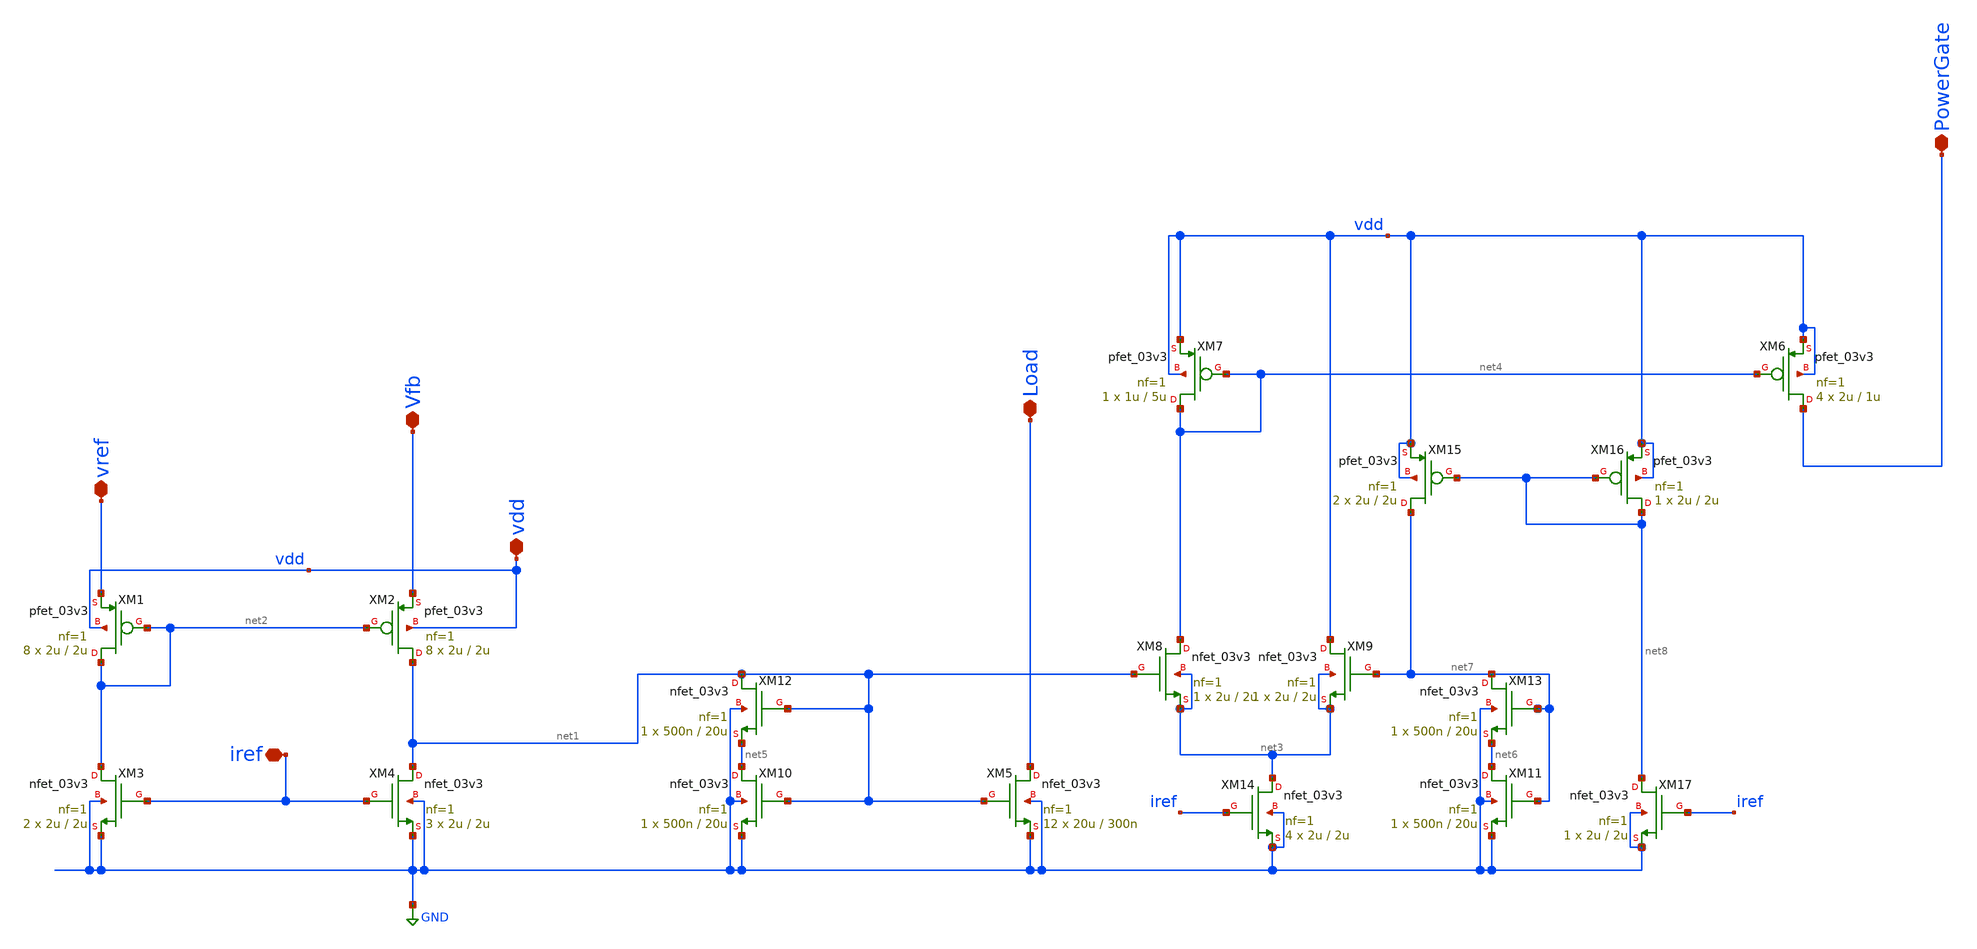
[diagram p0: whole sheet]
** sch_path: Voltage_Reference/LDO/overvoltageProtection.sch
**.subckt overvoltageProtection vref iref vdd Load Vfb PowerGate
*.iopin vref
*.iopin iref
*.iopin vdd
*.iopin Load
*.iopin Vfb
*.iopin PowerGate
XM2 net1 net2 Vfb vdd pfet_03v3 L=2u W=2u nf=1 ad='int((nf+1)/2) * W/nf * 0.18u' as='int((nf+2)/2) * W/nf * 0.18u'
+ pd='2*int((nf+1)/2) * (W/nf + 0.18u)' ps='2*int((nf+2)/2) * (W/nf + 0.18u)' nrd='0.18u / W' nrs='0.18u / W'
+ sa=0 sb=0 sd=0 m=8
XM4 net1 iref GND GND nfet_03v3 L=2u W=2u nf=1 ad='int((nf+1)/2) * W/nf * 0.18u' as='int((nf+2)/2) * W/nf * 0.18u'
+ pd='2*int((nf+1)/2) * (W/nf + 0.18u)' ps='2*int((nf+2)/2) * (W/nf + 0.18u)' nrd='0.18u / W' nrs='0.18u / W'
+ sa=0 sb=0 sd=0 m=3
XM5 Load net1 GND GND nfet_03v3 L=300n W=20u nf=1 ad='int((nf+1)/2) * W/nf * 0.18u' as='int((nf+2)/2) * W/nf * 0.18u'
+ pd='2*int((nf+1)/2) * (W/nf + 0.18u)' ps='2*int((nf+2)/2) * (W/nf + 0.18u)' nrd='0.18u / W' nrs='0.18u / W'
+ sa=0 sb=0 sd=0 m=12
XM1 net2 net2 vref vdd pfet_03v3 L=2u W=2u nf=1 ad='int((nf+1)/2) * W/nf * 0.18u' as='int((nf+2)/2) * W/nf * 0.18u'
+ pd='2*int((nf+1)/2) * (W/nf + 0.18u)' ps='2*int((nf+2)/2) * (W/nf + 0.18u)' nrd='0.18u / W' nrs='0.18u / W'
+ sa=0 sb=0 sd=0 m=8
XM3 net2 iref GND GND nfet_03v3 L=2u W=2u nf=1 ad='int((nf+1)/2) * W/nf * 0.18u' as='int((nf+2)/2) * W/nf * 0.18u'
+ pd='2*int((nf+1)/2) * (W/nf + 0.18u)' ps='2*int((nf+2)/2) * (W/nf + 0.18u)' nrd='0.18u / W' nrs='0.18u / W'
+ sa=0 sb=0 sd=0 m=2
XM6 PowerGate net4 vdd vdd pfet_03v3 L=1u W=2u nf=1 ad='int((nf+1)/2) * W/nf * 0.18u' as='int((nf+2)/2) * W/nf * 0.18u'
+ pd='2*int((nf+1)/2) * (W/nf + 0.18u)' ps='2*int((nf+2)/2) * (W/nf + 0.18u)' nrd='0.18u / W' nrs='0.18u / W'
+ sa=0 sb=0 sd=0 m=4
XM7 net4 net4 vdd vdd pfet_03v3 L=5u W=1u nf=1 ad='int((nf+1)/2) * W/nf * 0.18u' as='int((nf+2)/2) * W/nf * 0.18u'
+ pd='2*int((nf+1)/2) * (W/nf + 0.18u)' ps='2*int((nf+2)/2) * (W/nf + 0.18u)' nrd='0.18u / W' nrs='0.18u / W'
+ sa=0 sb=0 sd=0 m=1
XM8 net4 net1 net3 net3 nfet_03v3 L=2u W=2u nf=1 ad='int((nf+1)/2) * W/nf * 0.18u' as='int((nf+2)/2) * W/nf * 0.18u'
+ pd='2*int((nf+1)/2) * (W/nf + 0.18u)' ps='2*int((nf+2)/2) * (W/nf + 0.18u)' nrd='0.18u / W' nrs='0.18u / W'
+ sa=0 sb=0 sd=0 m=1
XM10 net5 net1 GND GND nfet_03v3 L=20u W=500n nf=1 ad='int((nf+1)/2) * W/nf * 0.18u' as='int((nf+2)/2) * W/nf * 0.18u'
+ pd='2*int((nf+1)/2) * (W/nf + 0.18u)' ps='2*int((nf+2)/2) * (W/nf + 0.18u)' nrd='0.18u / W' nrs='0.18u / W'
+ sa=0 sb=0 sd=0 m=1
XM12 net1 net1 net5 GND nfet_03v3 L=20u W=500n nf=1 ad='int((nf+1)/2) * W/nf * 0.18u' as='int((nf+2)/2) * W/nf * 0.18u'
+ pd='2*int((nf+1)/2) * (W/nf + 0.18u)' ps='2*int((nf+2)/2) * (W/nf + 0.18u)' nrd='0.18u / W' nrs='0.18u / W'
+ sa=0 sb=0 sd=0 m=1
XM9 vdd net7 net3 net3 nfet_03v3 L=2u W=2u nf=1 ad='int((nf+1)/2) * W/nf * 0.18u' as='int((nf+2)/2) * W/nf * 0.18u'
+ pd='2*int((nf+1)/2) * (W/nf + 0.18u)' ps='2*int((nf+2)/2) * (W/nf + 0.18u)' nrd='0.18u / W' nrs='0.18u / W'
+ sa=0 sb=0 sd=0 m=1
XM11 net6 net7 GND GND nfet_03v3 L=20u W=500n nf=1 ad='int((nf+1)/2) * W/nf * 0.18u' as='int((nf+2)/2) * W/nf * 0.18u'
+ pd='2*int((nf+1)/2) * (W/nf + 0.18u)' ps='2*int((nf+2)/2) * (W/nf + 0.18u)' nrd='0.18u / W' nrs='0.18u / W'
+ sa=0 sb=0 sd=0 m=1
XM13 net7 net7 net6 GND nfet_03v3 L=20u W=500n nf=1 ad='int((nf+1)/2) * W/nf * 0.18u' as='int((nf+2)/2) * W/nf * 0.18u'
+ pd='2*int((nf+1)/2) * (W/nf + 0.18u)' ps='2*int((nf+2)/2) * (W/nf + 0.18u)' nrd='0.18u / W' nrs='0.18u / W'
+ sa=0 sb=0 sd=0 m=1
XM14 net3 iref GND GND nfet_03v3 L=2u W=2u nf=1 ad='int((nf+1)/2) * W/nf * 0.18u' as='int((nf+2)/2) * W/nf * 0.18u'
+ pd='2*int((nf+1)/2) * (W/nf + 0.18u)' ps='2*int((nf+2)/2) * (W/nf + 0.18u)' nrd='0.18u / W' nrs='0.18u / W'
+ sa=0 sb=0 sd=0 m=4
XM15 net7 net8 vdd vdd pfet_03v3 L=2u W=2u nf=1 ad='int((nf+1)/2) * W/nf * 0.18u' as='int((nf+2)/2) * W/nf * 0.18u'
+ pd='2*int((nf+1)/2) * (W/nf + 0.18u)' ps='2*int((nf+2)/2) * (W/nf + 0.18u)' nrd='0.18u / W' nrs='0.18u / W'
+ sa=0 sb=0 sd=0 m=2
XM16 net8 net8 vdd vdd pfet_03v3 L=2u W=2u nf=1 ad='int((nf+1)/2) * W/nf * 0.18u' as='int((nf+2)/2) * W/nf * 0.18u'
+ pd='2*int((nf+1)/2) * (W/nf + 0.18u)' ps='2*int((nf+2)/2) * (W/nf + 0.18u)' nrd='0.18u / W' nrs='0.18u / W'
+ sa=0 sb=0 sd=0 m=1
XM17 net8 iref GND GND nfet_03v3 L=2u W=2u nf=1 ad='int((nf+1)/2) * W/nf * 0.18u' as='int((nf+2)/2) * W/nf * 0.18u'
+ pd='2*int((nf+1)/2) * (W/nf + 0.18u)' ps='2*int((nf+2)/2) * (W/nf + 0.18u)' nrd='0.18u / W' nrs='0.18u / W'
+ sa=0 sb=0 sd=0 m=1
**.ends
.GLOBAL GND
.end
